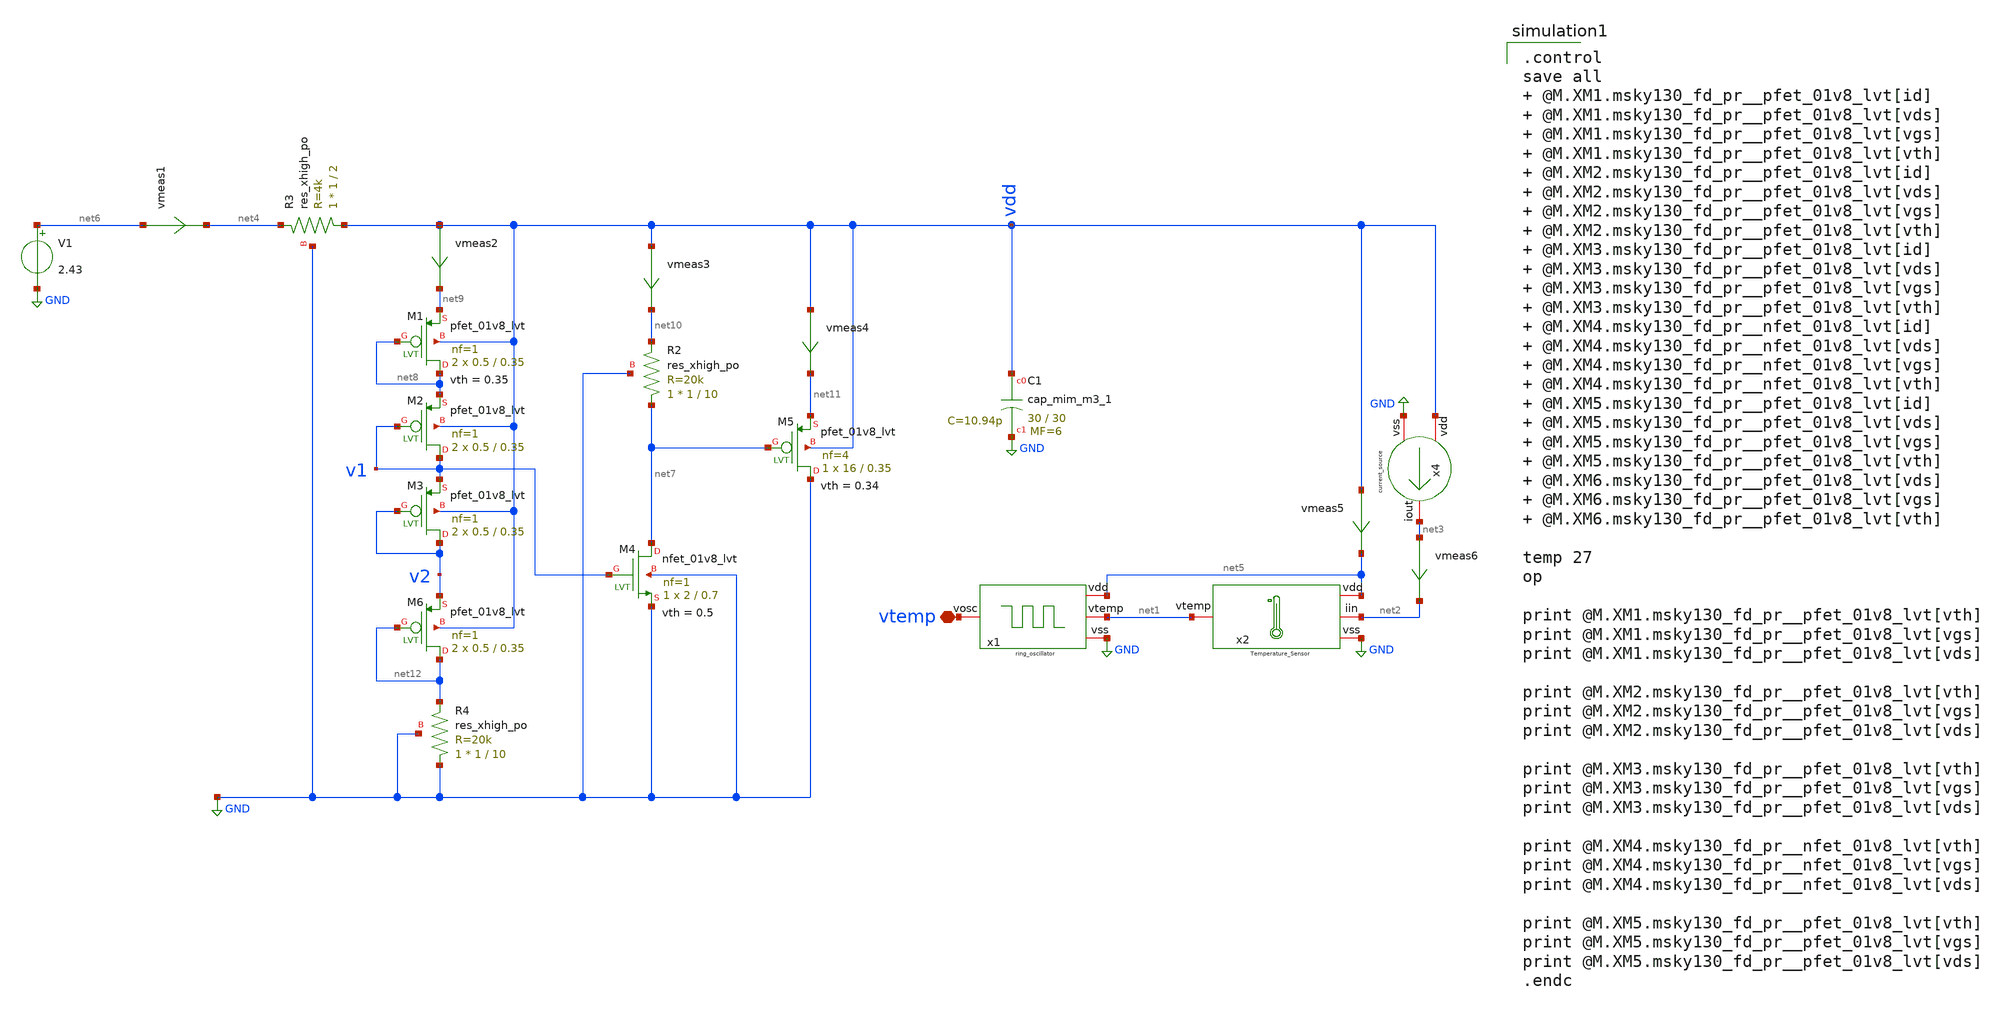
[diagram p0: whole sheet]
** sch_path: XSCHEM/prueba_vlim.sch
**.subckt prueba_vlim vtemp
*.iopin vtemp
vmeas6 net3 net2 0
.save i(vmeas6)
vmeas1 net6 net4 0
.save i(vmeas1)
vmeas5 vdd net5 0
.save i(vmeas5)
XC1 vdd GND sky130_fd_pr__cap_mim_m3_1 W=30 L=30 MF=6 m=6
x2 net5 net1 net2 GND Temperature_Sensor
x4 vdd net3 GND current_source
V1 net6 GND 2.43
XM4 net7 v1 GND GND sky130_fd_pr__nfet_01v8_lvt L=0.7 W=2 nf=1 ad='int((nf+1)/2) * W/nf * 0.29' as='int((nf+2)/2) * W/nf * 0.29'
+ pd='2*int((nf+1)/2) * (W/nf + 0.29)' ps='2*int((nf+2)/2) * (W/nf + 0.29)' nrd='0.29 / W' nrs='0.29 / W'
+ sa=0 sb=0 sd=0 mult=1 m=1
XM5 GND net7 net11 vdd sky130_fd_pr__pfet_01v8_lvt L=0.35 W=16 nf=4 ad='int((nf+1)/2) * W/nf * 0.29'
+ as='int((nf+2)/2) * W/nf * 0.29' pd='2*int((nf+1)/2) * (W/nf + 0.29)' ps='2*int((nf+2)/2) * (W/nf + 0.29)'
+ nrd='0.29 / W' nrs='0.29 / W' sa=0 sb=0 sd=0 mult=1 m=1
XM1 net8 net8 net9 vdd sky130_fd_pr__pfet_01v8_lvt L=0.35 W=0.5 nf=1 ad='int((nf+1)/2) * W/nf * 0.29'
+ as='int((nf+2)/2) * W/nf * 0.29' pd='2*int((nf+1)/2) * (W/nf + 0.29)' ps='2*int((nf+2)/2) * (W/nf + 0.29)'
+ nrd='0.29 / W' nrs='0.29 / W' sa=0 sb=0 sd=0 mult=2 m=2
XM2 v1 v1 net8 vdd sky130_fd_pr__pfet_01v8_lvt L=0.35 W=0.5 nf=1 ad='int((nf+1)/2) * W/nf * 0.29' as='int((nf+2)/2) * W/nf * 0.29'
+ pd='2*int((nf+1)/2) * (W/nf + 0.29)' ps='2*int((nf+2)/2) * (W/nf + 0.29)' nrd='0.29 / W' nrs='0.29 / W'
+ sa=0 sb=0 sd=0 mult=2 m=2
XM3 v2 v2 v1 vdd sky130_fd_pr__pfet_01v8_lvt L=0.35 W=0.5 nf=1 ad='int((nf+1)/2) * W/nf * 0.29' as='int((nf+2)/2) * W/nf * 0.29'
+ pd='2*int((nf+1)/2) * (W/nf + 0.29)' ps='2*int((nf+2)/2) * (W/nf + 0.29)' nrd='0.29 / W' nrs='0.29 / W'
+ sa=0 sb=0 sd=0 mult=2 m=2
XR3 vdd net4 GND sky130_fd_pr__res_xhigh_po W=1 L=2 mult=1 m=1
XR2 net7 net10 GND sky130_fd_pr__res_xhigh_po W=1 L=10 mult=1 m=1
XR4 GND net12 GND sky130_fd_pr__res_xhigh_po W=1 L=10 mult=1 m=1
x1 net5 vtemp GND net1 ring_oscillator
vmeas2 vdd net9 0
.save i(vmeas2)
vmeas3 vdd net10 0
.save i(vmeas3)
vmeas4 vdd net11 0
.save i(vmeas4)
XM6 net12 net12 v2 vdd sky130_fd_pr__pfet_01v8_lvt L=0.35 W=0.5 nf=1 ad='int((nf+1)/2) * W/nf * 0.29'
+ as='int((nf+2)/2) * W/nf * 0.29' pd='2*int((nf+1)/2) * (W/nf + 0.29)' ps='2*int((nf+2)/2) * (W/nf + 0.29)'
+ nrd='0.29 / W' nrs='0.29 / W' sa=0 sb=0 sd=0 mult=2 m=2
**** begin user architecture code

** opencircuitdesign pdks install
.lib $::SKYWATER_MODELS/sky130.lib.spice tt



.control
save all  @M.XM1.msky130_fd_pr__pfet_01v8_lvt[id]  @M.XM1.msky130_fd_pr__pfet_01v8_lvt[vds]
+  @M.XM1.msky130_fd_pr__pfet_01v8_lvt[vgs]  @M.XM1.msky130_fd_pr__pfet_01v8_lvt[vth]  @M.XM2.msky130_fd_pr__pfet_01v8_lvt[id]
+  @M.XM2.msky130_fd_pr__pfet_01v8_lvt[vds]  @M.XM2.msky130_fd_pr__pfet_01v8_lvt[vgs]  @M.XM2.msky130_fd_pr__pfet_01v8_lvt[vth]
+  @M.XM3.msky130_fd_pr__pfet_01v8_lvt[id]  @M.XM3.msky130_fd_pr__pfet_01v8_lvt[vds]  @M.XM3.msky130_fd_pr__pfet_01v8_lvt[vgs]
+  @M.XM3.msky130_fd_pr__pfet_01v8_lvt[vth]  @M.XM4.msky130_fd_pr__nfet_01v8_lvt[id]  @M.XM4.msky130_fd_pr__nfet_01v8_lvt[vds]
+  @M.XM4.msky130_fd_pr__nfet_01v8_lvt[vgs]  @M.XM4.msky130_fd_pr__nfet_01v8_lvt[vth]  @M.XM5.msky130_fd_pr__pfet_01v8_lvt[id]
+  @M.XM5.msky130_fd_pr__pfet_01v8_lvt[vds]  @M.XM5.msky130_fd_pr__pfet_01v8_lvt[vgs]  @M.XM5.msky130_fd_pr__pfet_01v8_lvt[vth]
+  @M.XM6.msky130_fd_pr__pfet_01v8_lvt[vds]  @M.XM6.msky130_fd_pr__pfet_01v8_lvt[vgs]  @M.XM6.msky130_fd_pr__pfet_01v8_lvt[vth]

temp 27
op

print @M.XM1.msky130_fd_pr__pfet_01v8_lvt[vth]
print @M.XM1.msky130_fd_pr__pfet_01v8_lvt[vgs]
print @M.XM1.msky130_fd_pr__pfet_01v8_lvt[vds]

print @M.XM2.msky130_fd_pr__pfet_01v8_lvt[vth]
print @M.XM2.msky130_fd_pr__pfet_01v8_lvt[vgs]
print @M.XM2.msky130_fd_pr__pfet_01v8_lvt[vds]

print @M.XM3.msky130_fd_pr__pfet_01v8_lvt[vth]
print @M.XM3.msky130_fd_pr__pfet_01v8_lvt[vgs]
print @M.XM3.msky130_fd_pr__pfet_01v8_lvt[vds]

print @M.XM4.msky130_fd_pr__nfet_01v8_lvt[vth]
print @M.XM4.msky130_fd_pr__nfet_01v8_lvt[vgs]
print @M.XM4.msky130_fd_pr__nfet_01v8_lvt[vds]

print @M.XM5.msky130_fd_pr__pfet_01v8_lvt[vth]
print @M.XM5.msky130_fd_pr__pfet_01v8_lvt[vgs]
print @M.XM5.msky130_fd_pr__pfet_01v8_lvt[vds]
.endc

**** end user architecture code
**.ends
.GLOBAL GND
.end
